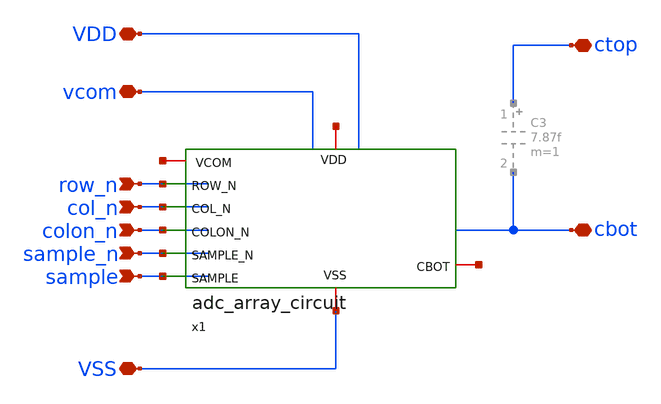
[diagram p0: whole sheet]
** sch_path: xschem/adc_array_cap_150n/adc_array_cap.sch
**.subckt adc_array_cap sample_n sample vcom row_n col_n colon_n VDD ctop VSS cbot
*.ipin sample_n
*.ipin sample
*.iopin vcom
*.ipin row_n
*.ipin col_n
*.ipin colon_n
*.iopin VDD
*.iopin ctop
*.iopin VSS
*.iopin cbot
x1 net1 row_n net2 col_n colon_n sample_n net3 sample VSS adc_array_circuit
**.ends

* expanding   symbol:  adc_array_circuit.sym # of pins=9
** sym_path: xschem/adc_array_cap/adc_array_circuit.sym
** sch_path: xschem/adc_array_cap/adc_array_circuit.sch
.subckt adc_array_circuit VDD ROW_N CBOT COL_N COLON_N SAMPLE_N VCOM SAMPLE VSS
*.ipin SAMPLE_N
*.ipin SAMPLE
*.iopin VCOM
*.ipin ROW_N
*.ipin COL_N
*.ipin COLON_N
*.iopin VDD
*.iopin VSS
*.iopin CBOT
XM1 VCOM SAMPLE CBOT VSS sky130_fd_pr__nfet_01v8 L=0.18 W=0.42 nf=1 ad='int((nf+1)/2) * W/nf * 0.29'
+ as='int((nf+2)/2) * W/nf * 0.29' pd='2*int((nf+1)/2) * (W/nf + 0.29)' ps='2*int((nf+2)/2) * (W/nf + 0.29)'
+ nrd='0.29 / W' nrs='0.29 / W' sa=0 sb=0 sd=0 mult=1 m=1
XM3 VCOM SAMPLE_N CBOT VDD sky130_fd_pr__pfet_01v8 L=0.18 W=0.9 nf=1 ad='int((nf+1)/2) * W/nf * 0.29'
+ as='int((nf+2)/2) * W/nf * 0.29' pd='2*int((nf+1)/2) * (W/nf + 0.29)' ps='2*int((nf+2)/2) * (W/nf + 0.29)'
+ nrd='0.29 / W' nrs='0.29 / W' sa=0 sb=0 sd=0 mult=1 m=1
XM2 VDRV SAMPLE_N CBOT VSS sky130_fd_pr__nfet_01v8 L=0.18 W=0.42 nf=1 ad='int((nf+1)/2) * W/nf * 0.29'
+ as='int((nf+2)/2) * W/nf * 0.29' pd='2*int((nf+1)/2) * (W/nf + 0.29)' ps='2*int((nf+2)/2) * (W/nf + 0.29)'
+ nrd='0.29 / W' nrs='0.29 / W' sa=0 sb=0 sd=0 mult=1 m=1
XM4 VDRV SAMPLE CBOT VDD sky130_fd_pr__pfet_01v8 L=0.18 W=0.9 nf=1 ad='int((nf+1)/2) * W/nf * 0.29' as='int((nf+2)/2) * W/nf * 0.29'
+ pd='2*int((nf+1)/2) * (W/nf + 0.29)' ps='2*int((nf+2)/2) * (W/nf + 0.29)' nrd='0.29 / W' nrs='0.29 / W'
+ sa=0 sb=0 sd=0 mult=1 m=1
XM5 VINT1 COL_N VDRV VDD sky130_fd_pr__pfet_01v8 L=0.18 W=0.9 nf=1 ad='int((nf+1)/2) * W/nf * 0.29' as='int((nf+2)/2) * W/nf * 0.29'
+ pd='2*int((nf+1)/2) * (W/nf + 0.29)' ps='2*int((nf+2)/2) * (W/nf + 0.29)' nrd='0.29 / W' nrs='0.29 / W'
+ sa=0 sb=0 sd=0 mult=1 m=1
XM6 VDD ROW_N VINT1 VDD sky130_fd_pr__pfet_01v8 L=0.18 W=0.9 nf=1 ad='int((nf+1)/2) * W/nf * 0.29' as='int((nf+2)/2) * W/nf * 0.29'
+ pd='2*int((nf+1)/2) * (W/nf + 0.29)' ps='2*int((nf+2)/2) * (W/nf + 0.29)' nrd='0.29 / W' nrs='0.29 / W'
+ sa=0 sb=0 sd=0 mult=1 m=1
XM7 VDD COLON_N VDRV VDD sky130_fd_pr__pfet_01v8 L=0.18 W=0.9 nf=1 ad='int((nf+1)/2) * W/nf * 0.29' as='int((nf+2)/2) * W/nf * 0.29'
+ pd='2*int((nf+1)/2) * (W/nf + 0.29)' ps='2*int((nf+2)/2) * (W/nf + 0.29)' nrd='0.29 / W' nrs='0.29 / W'
+ sa=0 sb=0 sd=0 mult=1 m=1
XM8 VINT2 COLON_N VDRV VSS sky130_fd_pr__nfet_01v8 L=0.18 W=0.42 nf=1 ad='int((nf+1)/2) * W/nf * 0.29'
+ as='int((nf+2)/2) * W/nf * 0.29' pd='2*int((nf+1)/2) * (W/nf + 0.29)' ps='2*int((nf+2)/2) * (W/nf + 0.29)'
+ nrd='0.29 / W' nrs='0.29 / W' sa=0 sb=0 sd=0 mult=1 m=1
XM9 VSS ROW_N VINT2 VSS sky130_fd_pr__nfet_01v8 L=0.18 W=0.42 nf=1 ad='int((nf+1)/2) * W/nf * 0.29' as='int((nf+2)/2) * W/nf * 0.29'
+ pd='2*int((nf+1)/2) * (W/nf + 0.29)' ps='2*int((nf+2)/2) * (W/nf + 0.29)' nrd='0.29 / W' nrs='0.29 / W'
+ sa=0 sb=0 sd=0 mult=1 m=1
XM10 VSS COL_N VINT2 VSS sky130_fd_pr__nfet_01v8 L=0.18 W=0.42 nf=1 ad='int((nf+1)/2) * W/nf * 0.29'
+ as='int((nf+2)/2) * W/nf * 0.29' pd='2*int((nf+1)/2) * (W/nf + 0.29)' ps='2*int((nf+2)/2) * (W/nf + 0.29)'
+ nrd='0.29 / W' nrs='0.29 / W' sa=0 sb=0 sd=0 mult=1 m=1
C0 COLON_N COL_N 1.23f m=1
C1 VDRV COL_N 0.98f m=1
C2 SAMPLE_N VDD 1.16f m=1
C VCOM VSS 1.65f m=1
C5 ROW_N VSS 1.02f m=1
C6 VDD VSS 2.65f m=1
C3 COLON_N SAMPLE 0.69f m=1
.ends

.end
